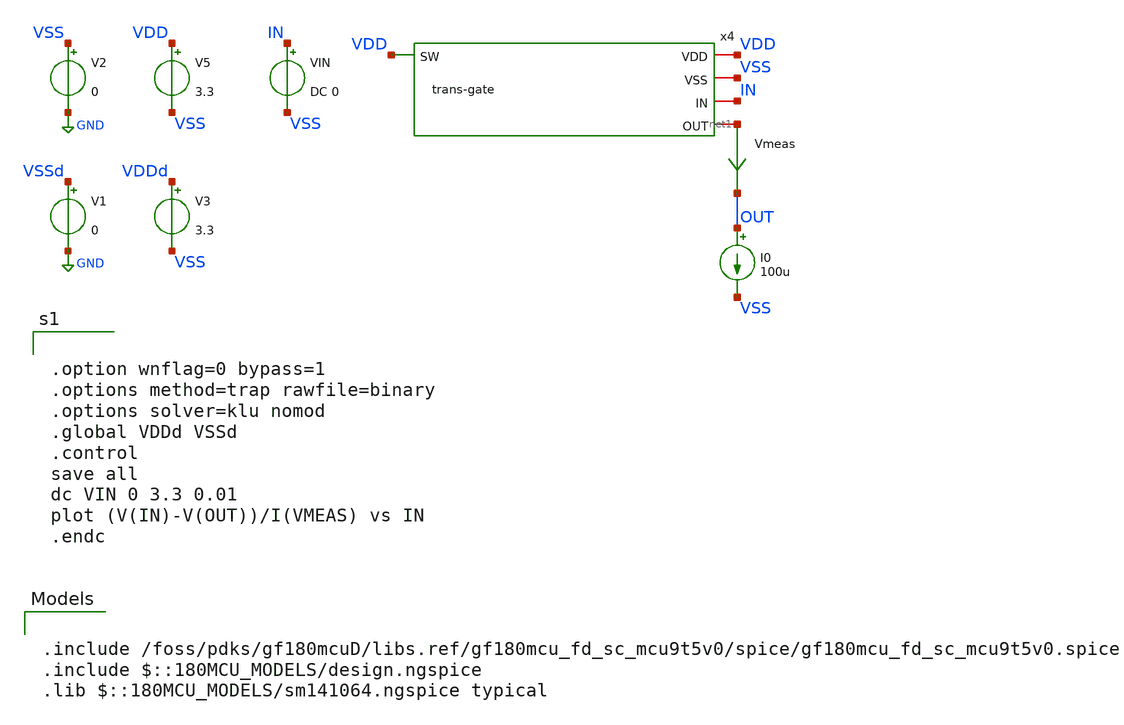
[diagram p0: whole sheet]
** sch_path: designs/libs/switch-matrix/tb_switch-matrix/tb_switch-matrix_tg.sch
**.subckt tb_switch-matrix_tg
V2 VSS GND 0
V5 VDD VSS 3.3
VIN IN VSS DC 0
Vmeas net1 OUT 0
.save i(vmeas)
I0 OUT VSS 100u
V1 VSSd GND 0
V3 VDDd VSS 3.3
x4 VDD VSS VDD IN net1 trans-gate
**** begin user architecture code


.option wnflag=0 bypass=1
.options method=trap rawfile=binary
.options solver=klu nomod
.global VDDd VSSd
.control
save all
dc VIN 0 3.3 0.01
plot (V(IN)-V(OUT))/I(VMEAS) vs IN
.endc



.include /foss/pdks/gf180mcuD/libs.ref/gf180mcu_fd_sc_mcu9t5v0/spice/gf180mcu_fd_sc_mcu9t5v0.spice
.include $::180MCU_MODELS/design.ngspice
.lib $::180MCU_MODELS/sm141064.ngspice typical

**** end user architecture code
**.ends
.GLOBAL GND
.end
